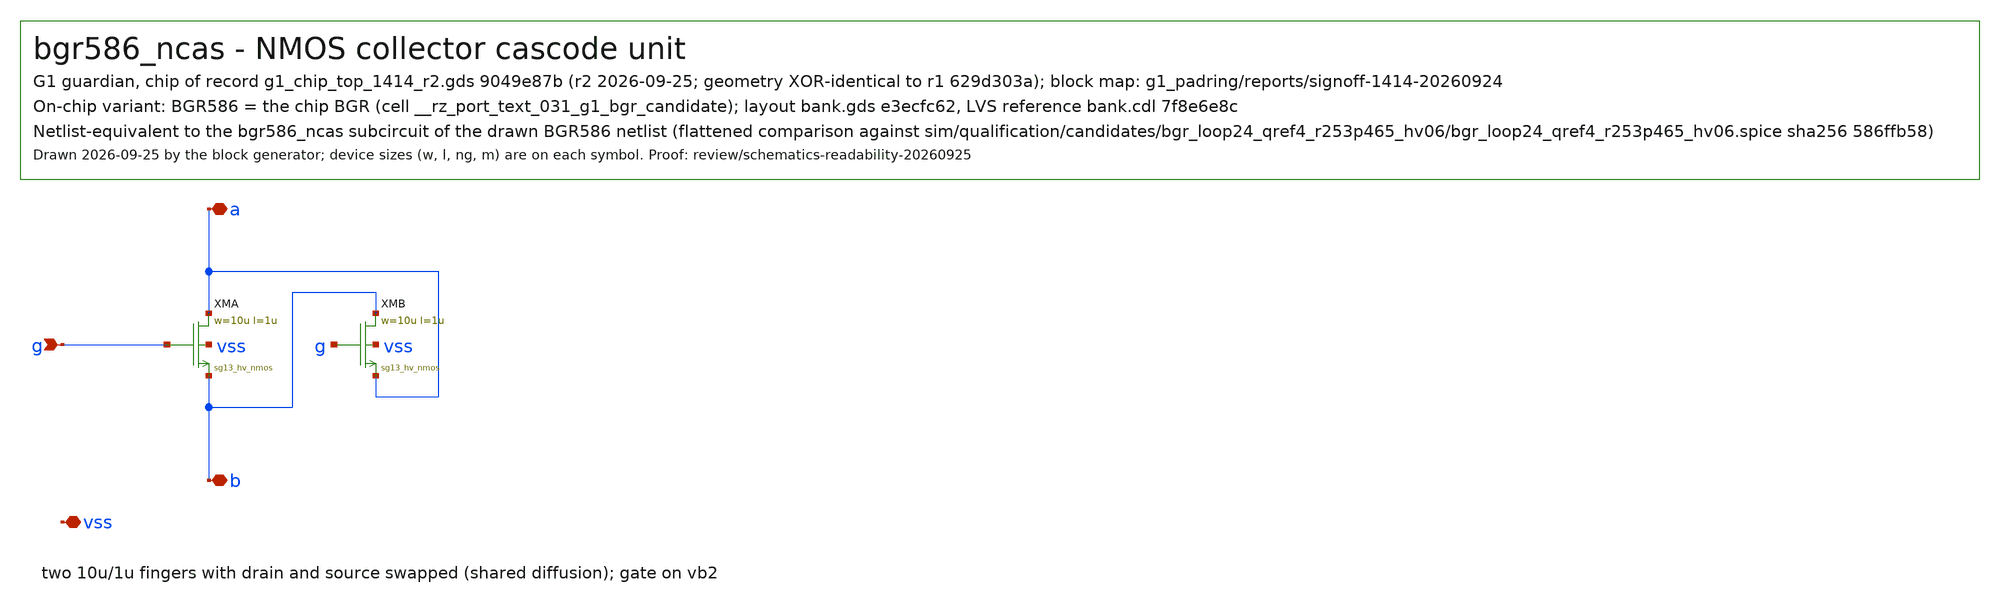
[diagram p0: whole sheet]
** sch_path: designs/g1-guardian/blocks/g1_bgr/xschem/bgr586/bgr586_ncas.sch
**.subckt bgr586_ncas a b g vss
*.iopin a
*.iopin b
*.ipin g
*.iopin vss
XMA a g b vss sg13_hv_nmos l=1u w=10u as=3.4p ad=3.4p ps=20.68u pd=20.68u rfmode=0
XMB b g a vss sg13_hv_nmos l=1u w=10u as=3.4p ad=3.4p ps=20.68u pd=20.68u rfmode=0
**.ends
.end
